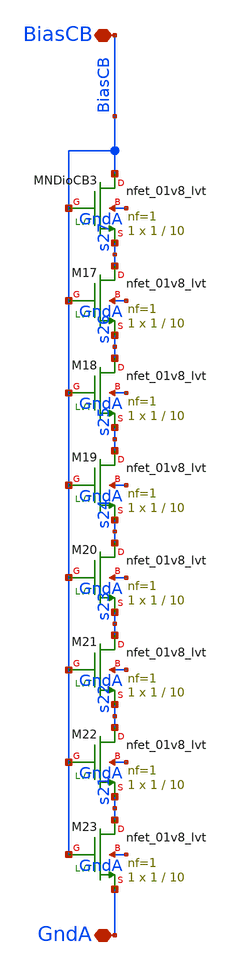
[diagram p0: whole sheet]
** sch_path: analog/xschem/BiasCoarseMB_DIV_W010_L100_8.sch
**.subckt BiasCoarseMB_DIV_W010_L100_8 BiasCB GndA
*.iopin BiasCB
*.iopin GndA
XMNDioCB3 BiasCB BiasCB s27 GndA sky130_fd_pr__nfet_01v8_lvt L=10 W=1 nf=1 ad='int((1 + 1)/2) * 1 / 1 * 0.29'
+ as='int((1 + 2)/2) * 1 / 1 * 0.29' pd='2*int((1 + 1)/2) * (1 / 1 + 0.29)' ps='2*int((1 + 2)/2) * (1 / 1 + 0.29)'
+ nrd='0.29 / 1 ' nrs='0.29 / 1 ' sa=0 sb=0 sd=0 mult=1 m=1
XM17 s27 BiasCB s26 GndA sky130_fd_pr__nfet_01v8_lvt L=10 W=1 nf=1 ad='int((1 + 1)/2) * 1 / 1 * 0.29'
+ as='int((1 + 2)/2) * 1 / 1 * 0.29' pd='2*int((1 + 1)/2) * (1 / 1 + 0.29)' ps='2*int((1 + 2)/2) * (1 / 1 + 0.29)'
+ nrd='0.29 / 1 ' nrs='0.29 / 1 ' sa=0 sb=0 sd=0 mult=1 m=1
XM18 s26 BiasCB s25 GndA sky130_fd_pr__nfet_01v8_lvt L=10 W=1 nf=1 ad='int((1 + 1)/2) * 1 / 1 * 0.29'
+ as='int((1 + 2)/2) * 1 / 1 * 0.29' pd='2*int((1 + 1)/2) * (1 / 1 + 0.29)' ps='2*int((1 + 2)/2) * (1 / 1 + 0.29)'
+ nrd='0.29 / 1 ' nrs='0.29 / 1 ' sa=0 sb=0 sd=0 mult=1 m=1
XM19 s25 BiasCB s24 GndA sky130_fd_pr__nfet_01v8_lvt L=10 W=1 nf=1 ad='int((1 + 1)/2) * 1 / 1 * 0.29'
+ as='int((1 + 2)/2) * 1 / 1 * 0.29' pd='2*int((1 + 1)/2) * (1 / 1 + 0.29)' ps='2*int((1 + 2)/2) * (1 / 1 + 0.29)'
+ nrd='0.29 / 1 ' nrs='0.29 / 1 ' sa=0 sb=0 sd=0 mult=1 m=1
XM20 s24 BiasCB s23 GndA sky130_fd_pr__nfet_01v8_lvt L=10 W=1 nf=1 ad='int((1 + 1)/2) * 1 / 1 * 0.29'
+ as='int((1 + 2)/2) * 1 / 1 * 0.29' pd='2*int((1 + 1)/2) * (1 / 1 + 0.29)' ps='2*int((1 + 2)/2) * (1 / 1 + 0.29)'
+ nrd='0.29 / 1 ' nrs='0.29 / 1 ' sa=0 sb=0 sd=0 mult=1 m=1
XM21 s23 BiasCB s22 GndA sky130_fd_pr__nfet_01v8_lvt L=10 W=1 nf=1 ad='int((1 + 1)/2) * 1 / 1 * 0.29'
+ as='int((1 + 2)/2) * 1 / 1 * 0.29' pd='2*int((1 + 1)/2) * (1 / 1 + 0.29)' ps='2*int((1 + 2)/2) * (1 / 1 + 0.29)'
+ nrd='0.29 / 1 ' nrs='0.29 / 1 ' sa=0 sb=0 sd=0 mult=1 m=1
XM22 s22 BiasCB s21 GndA sky130_fd_pr__nfet_01v8_lvt L=10 W=1 nf=1 ad='int((1 + 1)/2) * 1 / 1 * 0.29'
+ as='int((1 + 2)/2) * 1 / 1 * 0.29' pd='2*int((1 + 1)/2) * (1 / 1 + 0.29)' ps='2*int((1 + 2)/2) * (1 / 1 + 0.29)'
+ nrd='0.29 / 1 ' nrs='0.29 / 1 ' sa=0 sb=0 sd=0 mult=1 m=1
XM23 s21 BiasCB GndA GndA sky130_fd_pr__nfet_01v8_lvt L=10 W=1 nf=1 ad='int((1 + 1)/2) * 1 / 1 * 0.29'
+ as='int((1 + 2)/2) * 1 / 1 * 0.29' pd='2*int((1 + 1)/2) * (1 / 1 + 0.29)' ps='2*int((1 + 2)/2) * (1 / 1 + 0.29)'
+ nrd='0.29 / 1 ' nrs='0.29 / 1 ' sa=0 sb=0 sd=0 mult=1 m=1
**.ends
.end
